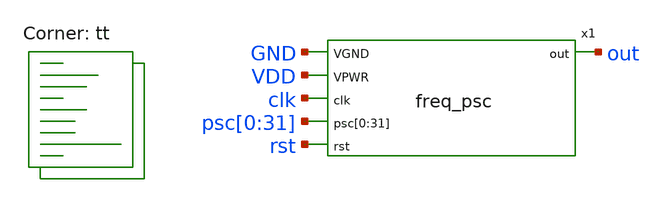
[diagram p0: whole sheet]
** sch_path: xschem/freq_psc-tb.sch
**.subckt freq_psc-tb
x1 GND VDD clk out psc[0] psc[1] psc[2] psc[3] psc[4] psc[5] psc[6] psc[7] psc[8] psc[9] psc[10]
+ psc[11] psc[12] psc[13] psc[14] psc[15] psc[16] psc[17] psc[18] psc[19] psc[20] psc[21] psc[22] psc[23]
+ psc[24] psc[25] psc[26] psc[27] psc[28] psc[29] psc[30] psc[31] rst freq_psc
**** begin user architecture code
 .lib $::SKYWATER_MODELS/sky130.lib.spice tt
.include $::SKYWATER_STDCELLS/sky130_fd_sc_hd.spice
.include $::SKYWATER_STDCELLS/sky130_ef_sc_hd__decap_12.spice
.include $::SKYWATER_STDCELLS/sky130_ef_sc_hd__fill_4.spice
.include $::SKYWATER_STDCELLS/sky130_ef_sc_hd__fill_8.spice
.include $::SKYWATER_STDCELLS/sky130_ef_sc_hd__fill_12.spice
.param mc_mm_switch = 0
.param mc_pr_switch = 0




  .include ~/gits/dsrt_2024/sky130_its_biomedical_chip_research_2024/spice/freq_psc.spice
  .param max_freq=100e6 period={1/max_freq} time_high={period/2}
  .param delay_vin1={time_high} delay_vin2={time_high*1.5}

  .option wnflag=1
  .option safecurrents

  *Vvdd  VDDA  VSS dc 1.8
  Vvdd1 VDD   GND dc 1.8
  Vin1 clk GND pulse(0 1.8 {delay_vin1} 1p 1p {time_high} {period})

  Vpsc0  psc[0] gnd dc 1.8
  Vpsc1  psc[1] gnd dc 0
  Vpsc2  psc[2] gnd dc 1.8
  Vpsc3  psc[3] gnd dc 0
  Vpsc4  psc[4] gnd dc 0
  Vpsc5  psc[5] gnd dc 0
  Vpsc6  psc[6] gnd dc 0
  Vpsc7  psc[7] gnd dc 0
  Vpsc8  psc[8] gnd dc 0
  Vpsc9  psc[9] gnd dc 0
  Vpsc10 psc[10] gnd dc 0
  Vpsc11 psc[11] gnd dc 0
  Vpsc12 psc[12] gnd dc 0
  Vpsc13 psc[13] gnd dc 0
  Vpsc14 psc[14] gnd dc 0
  Vpsc15 psc[15] gnd dc 0
  Vpsc16 psc[16] gnd dc 0
  Vpsc17 psc[17] gnd dc 0
  Vpsc18 psc[18] gnd dc 0
  Vpsc19 psc[19] gnd dc 0
  Vpsc20 psc[20] gnd dc 0
  Vpsc21 psc[21] gnd dc 0
  Vpsc22 psc[22] gnd dc 0
  Vpsc23 psc[23] gnd dc 0
  Vpsc24 psc[24] gnd dc 0
  Vpsc25 psc[25] gnd dc 0
  Vpsc26 psc[26] gnd dc 0
  Vpsc27 psc[27] gnd dc 0
  Vpsc28 psc[28] gnd dc 0
  Vpsc29 psc[29] gnd dc 0
  Vpsc30 psc[30] gnd dc 0
  Vpsc31 psc[31] gnd dc 0

  .control
     reset
     save all
     tran 0.01n 100n uic
     remzerovec
     write freq_psc-tb.raw
    quit 0
  .endc



**** end user architecture code
**.ends
.end
